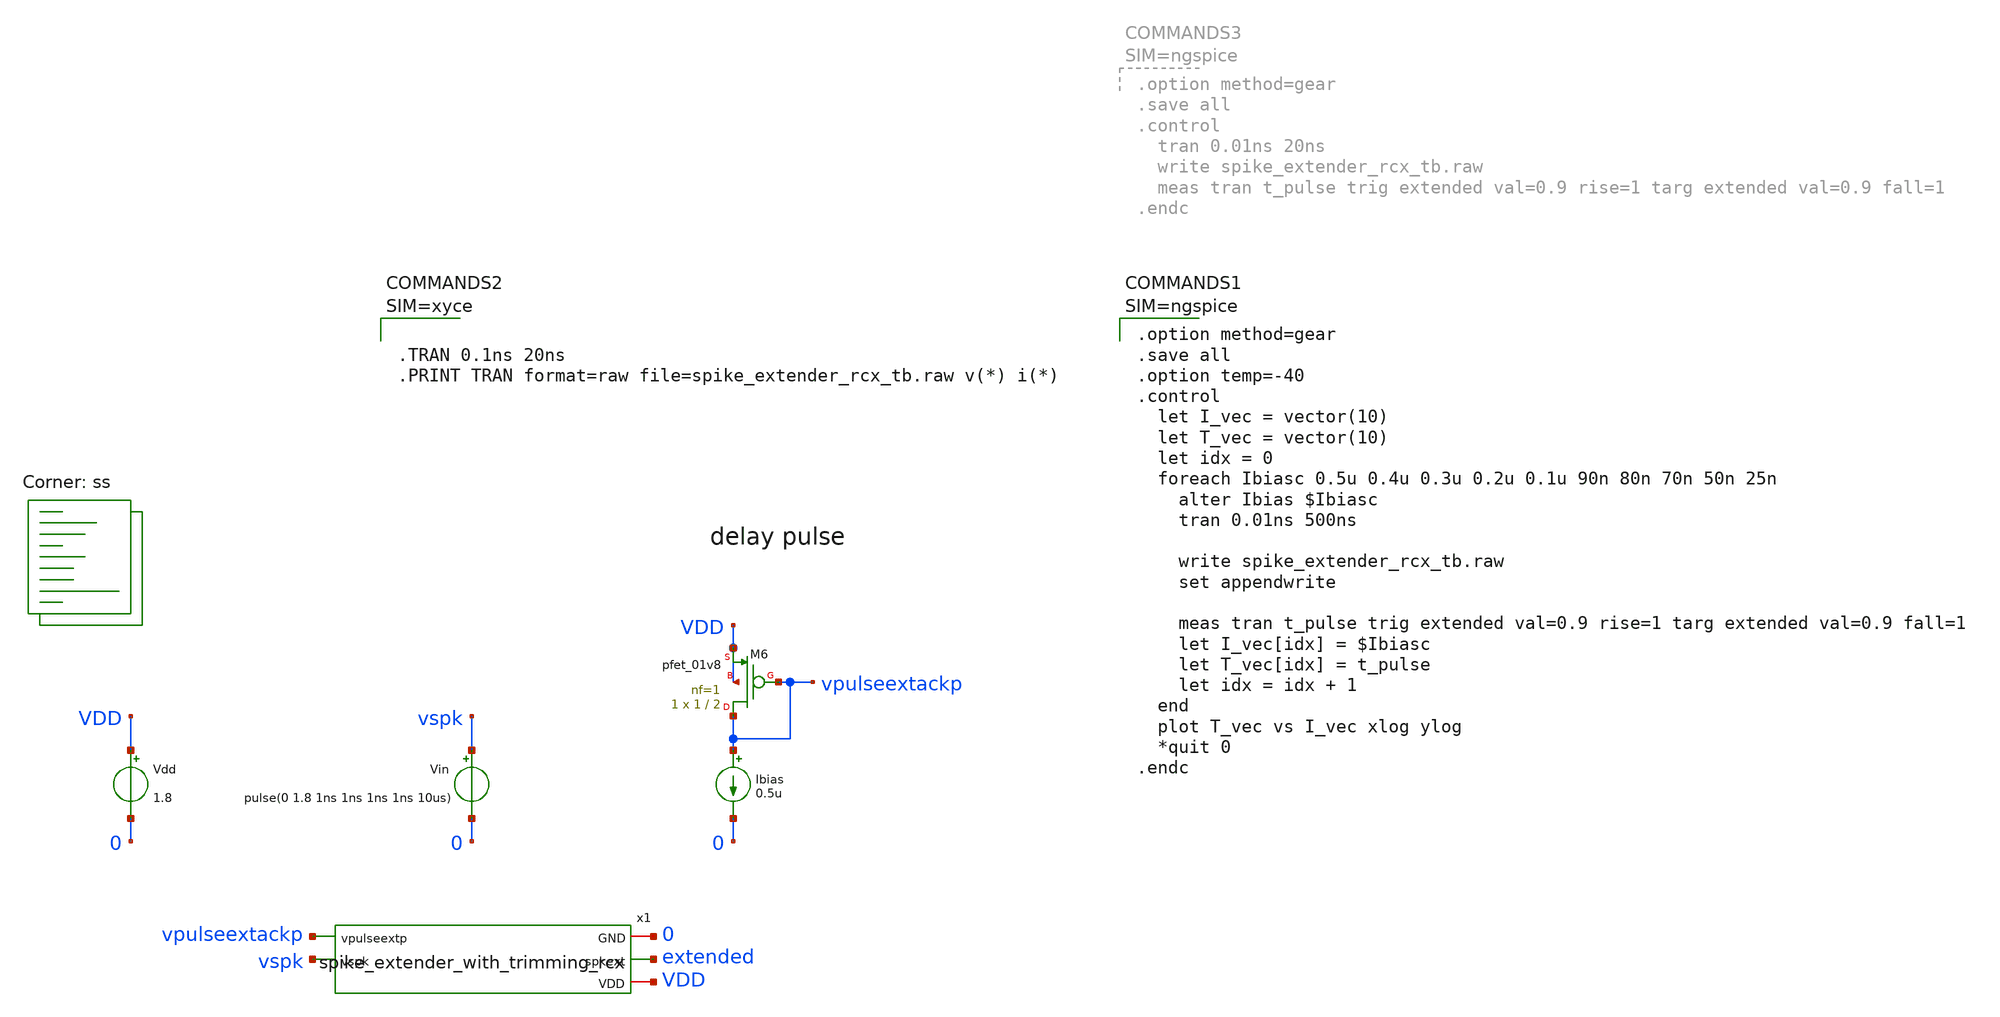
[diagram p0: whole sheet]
** sch_path: design/xschem/layout_tb/spike_extender_rcx_tb.sch
**.subckt spike_extender_rcx_tb
Vdd VDD 0 1.8
Vin vspk 0 pulse(0 1.8 1ns 1ns 1ns 1ns 10us)
XM6 vpulseextackp vpulseextackp VDD VDD sky130_fd_pr__pfet_01v8 L=2 W=1 nf=1 ad='int((nf+1)/2) * W/nf * 0.29'
+ as='int((nf+2)/2) * W/nf * 0.29' pd='2*int((nf+1)/2) * (W/nf + 0.29)' ps='2*int((nf+2)/2) * (W/nf + 0.29)'
+ nrd='0.29 / W' nrs='0.29 / W' sa=0 sb=0 sd=0 mult=1 m=1
Ibias vpulseextackp 0 0.5u
x1 vpulseextackp vspk 0 extended VDD spike_extender_with_trimming_rcx
**** begin user architecture code


* Standard cell simulation files
.include $::SKYWATER_STDCELLS/sky130_fd_sc_hd.spice

* Power domains
VSTDCELL_PWR VPWR 0 DC 1.8
VSTDCELL_PB  VPB  0 DC 1.8
VSTDCELL_NB  VNB  0 DC 0
VSTDCELL_GND VGND 0 DC 0
.global VNB VGND VPB VPWR


.lib $::SKYWATER_MODELS/sky130.lib.spice ss





.option method=gear
.save all
.option temp=-40
.control
  let I_vec = vector(10)
  let T_vec = vector(10)
  let idx = 0
  foreach Ibiasc 0.5u 0.4u 0.3u 0.2u 0.1u 90n 80n 70n 50n 25n
    alter Ibias $Ibiasc
    tran 0.01ns 500ns

    write spike_extender_rcx_tb.raw
    set appendwrite

    meas tran t_pulse trig extended val=0.9 rise=1 targ extended val=0.9 fall=1
    let I_vec[idx] = $Ibiasc
    let T_vec[idx] = t_pulse
    let idx = idx + 1
  end
  plot T_vec vs I_vec xlog ylog
  *quit 0
.endc



**** end user architecture code
**.ends

* expanding   symbol:  spike_extender_with_trimming_rcx.sym # of pins=5
** sym_path: design/xschem/spike_extender_with_trimming.sym
.include [abs_sym_path spike_extender_with_trimming_rcx.spice]
.end
